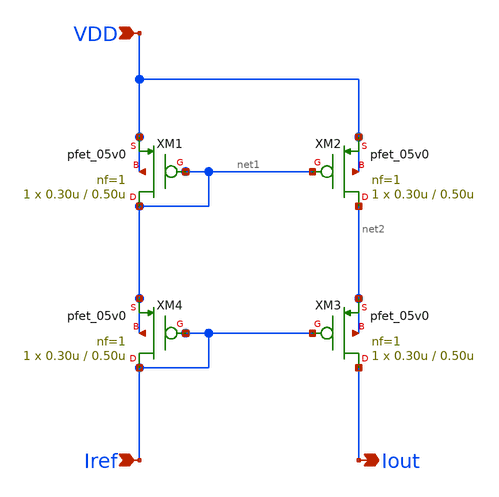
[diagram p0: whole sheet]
** sch_path: designs/libs/core_analog/current-mirror/pmos_current_mirror.sch
**.subckt pmos_current_mirror VDD Iref Iout
*.ipin VDD
*.ipin Iref
*.opin Iout
XM2 net2 net1 VDD VDD pfet_05v0 L=0.50u W=0.30u nf=1 ad='int((nf+1)/2) * W/nf * 0.18u' as='int((nf+2)/2) * W/nf * 0.18u'
+ pd='2*int((nf+1)/2) * (W/nf + 0.18u)' ps='2*int((nf+2)/2) * (W/nf + 0.18u)' nrd='0.18u / W' nrs='0.18u / W'
+ sa=0 sb=0 sd=0 m=1
XM1 net1 net1 VDD VDD pfet_05v0 L=0.50u W=0.30u nf=1 ad='int((nf+1)/2) * W/nf * 0.18u' as='int((nf+2)/2) * W/nf * 0.18u'
+ pd='2*int((nf+1)/2) * (W/nf + 0.18u)' ps='2*int((nf+2)/2) * (W/nf + 0.18u)' nrd='0.18u / W' nrs='0.18u / W'
+ sa=0 sb=0 sd=0 m=1
XM3 Iout Iref net2 net2 pfet_05v0 L=0.50u W=0.30u nf=1 ad='int((nf+1)/2) * W/nf * 0.18u' as='int((nf+2)/2) * W/nf * 0.18u'
+ pd='2*int((nf+1)/2) * (W/nf + 0.18u)' ps='2*int((nf+2)/2) * (W/nf + 0.18u)' nrd='0.18u / W' nrs='0.18u / W'
+ sa=0 sb=0 sd=0 m=1
XM4 Iref Iref net1 net1 pfet_05v0 L=0.50u W=0.30u nf=1 ad='int((nf+1)/2) * W/nf * 0.18u' as='int((nf+2)/2) * W/nf * 0.18u'
+ pd='2*int((nf+1)/2) * (W/nf + 0.18u)' ps='2*int((nf+2)/2) * (W/nf + 0.18u)' nrd='0.18u / W' nrs='0.18u / W'
+ sa=0 sb=0 sd=0 m=1
**.ends
.end
